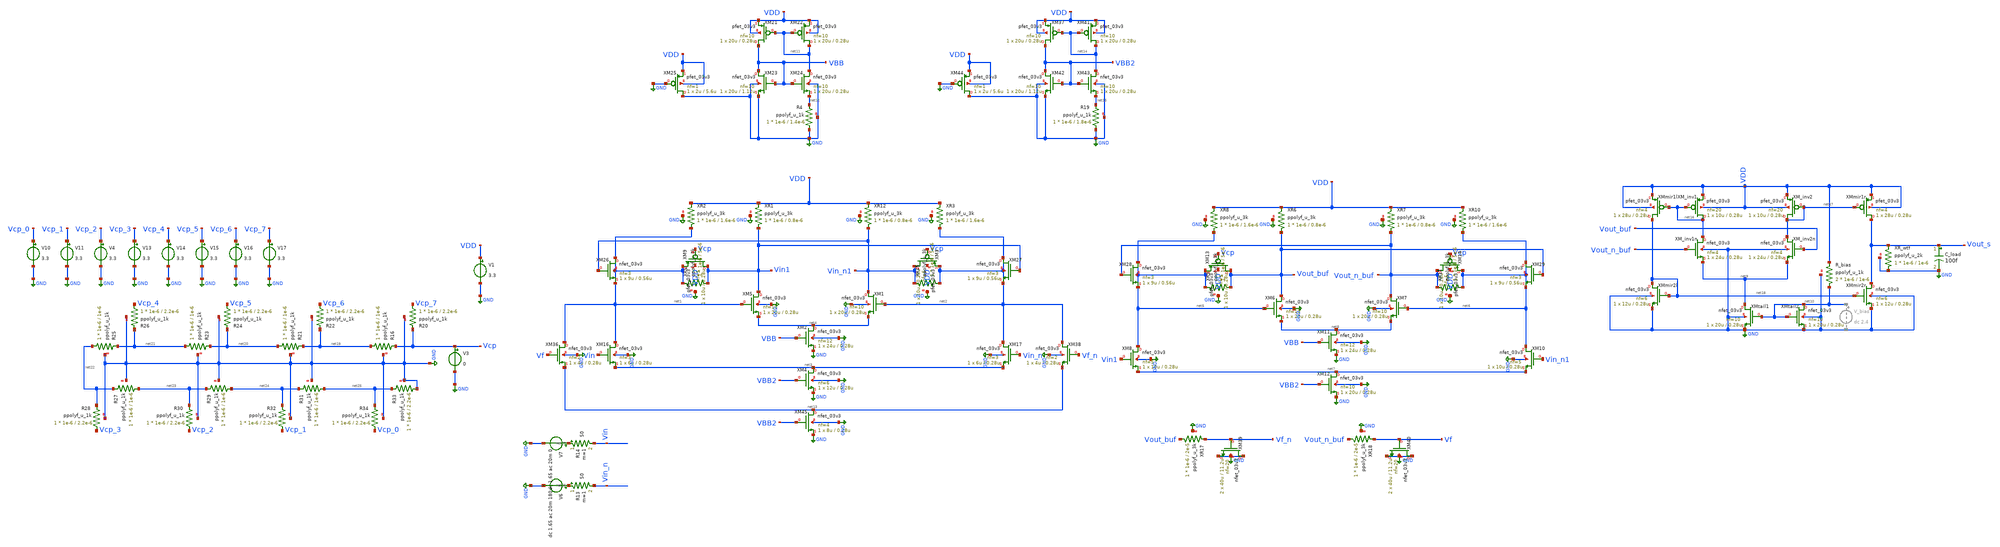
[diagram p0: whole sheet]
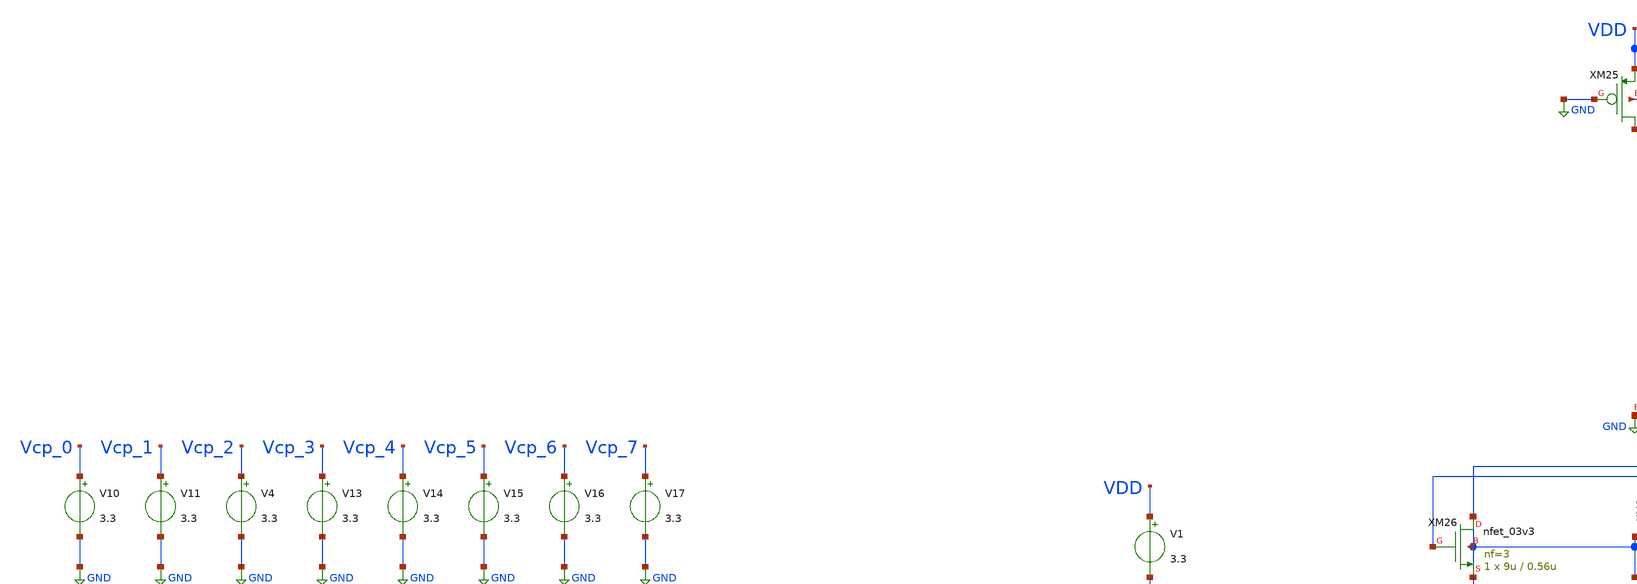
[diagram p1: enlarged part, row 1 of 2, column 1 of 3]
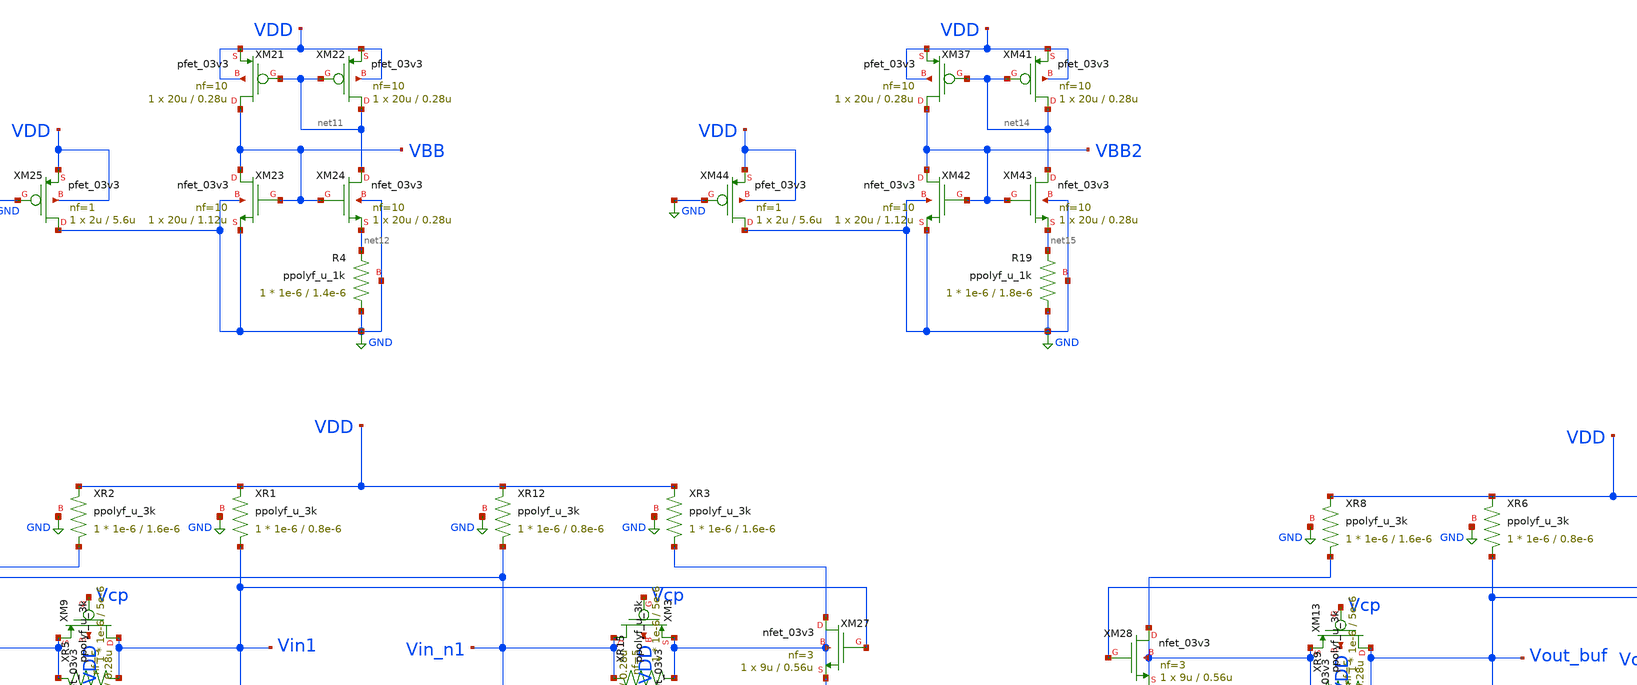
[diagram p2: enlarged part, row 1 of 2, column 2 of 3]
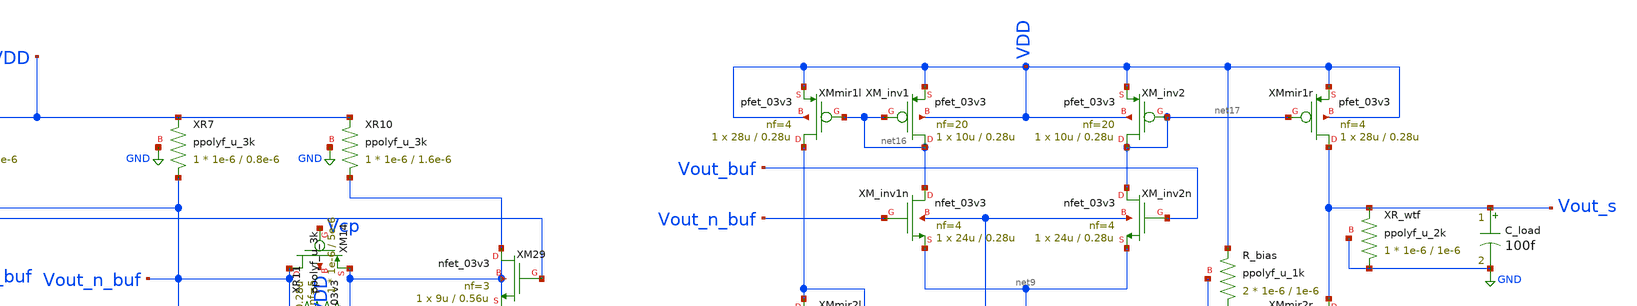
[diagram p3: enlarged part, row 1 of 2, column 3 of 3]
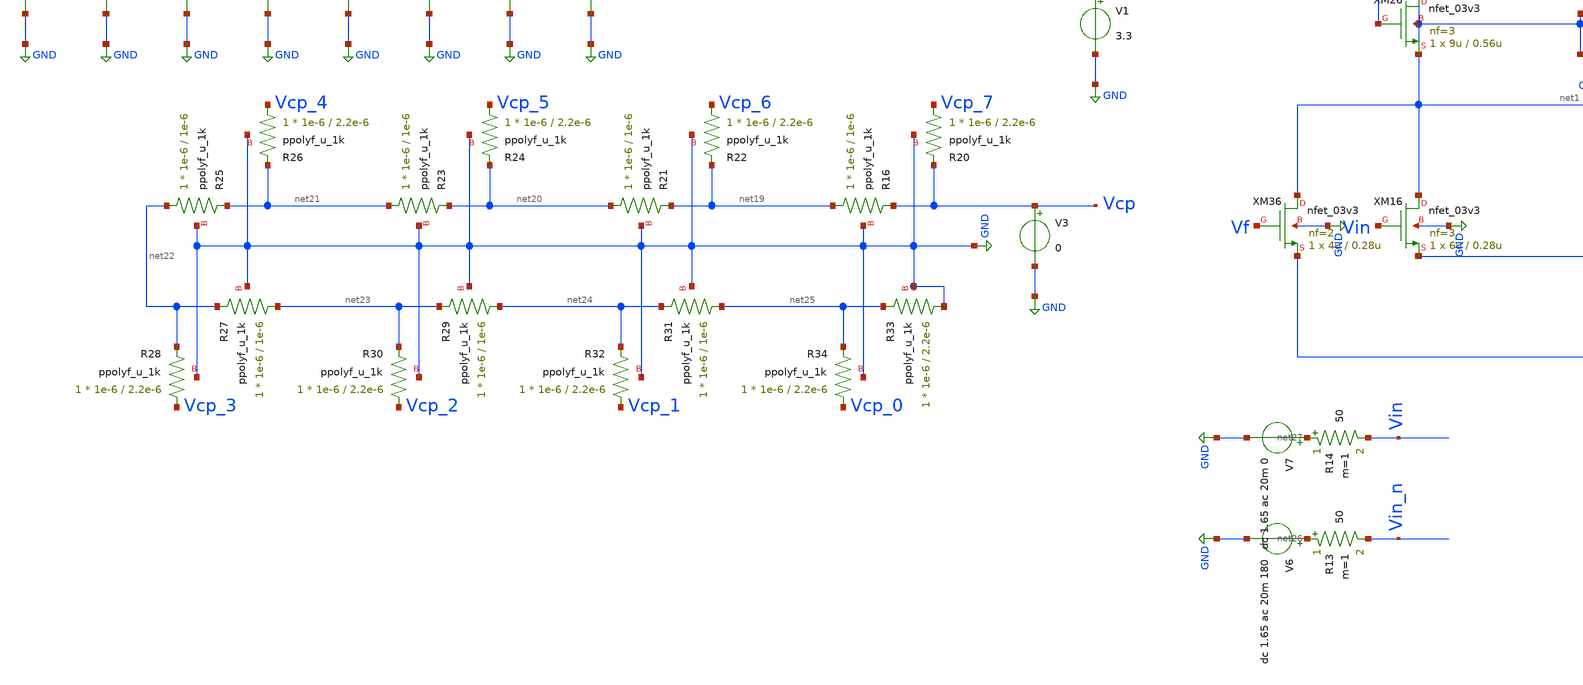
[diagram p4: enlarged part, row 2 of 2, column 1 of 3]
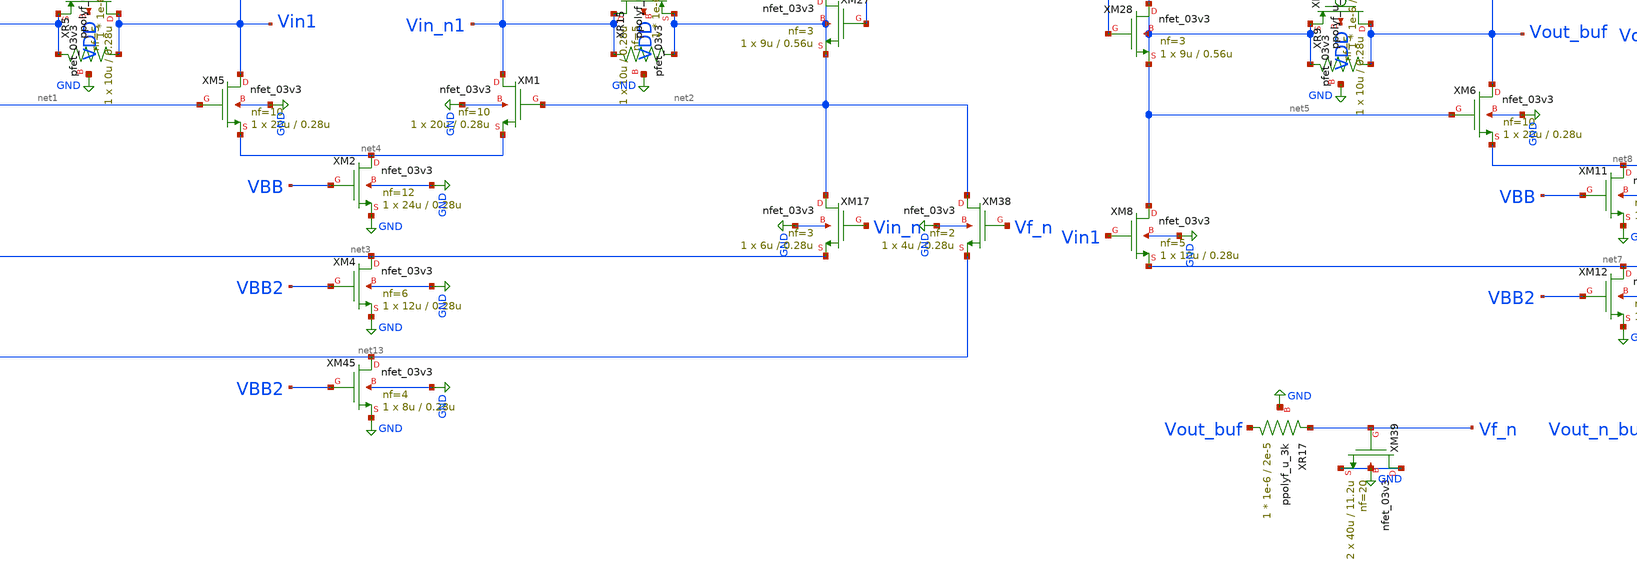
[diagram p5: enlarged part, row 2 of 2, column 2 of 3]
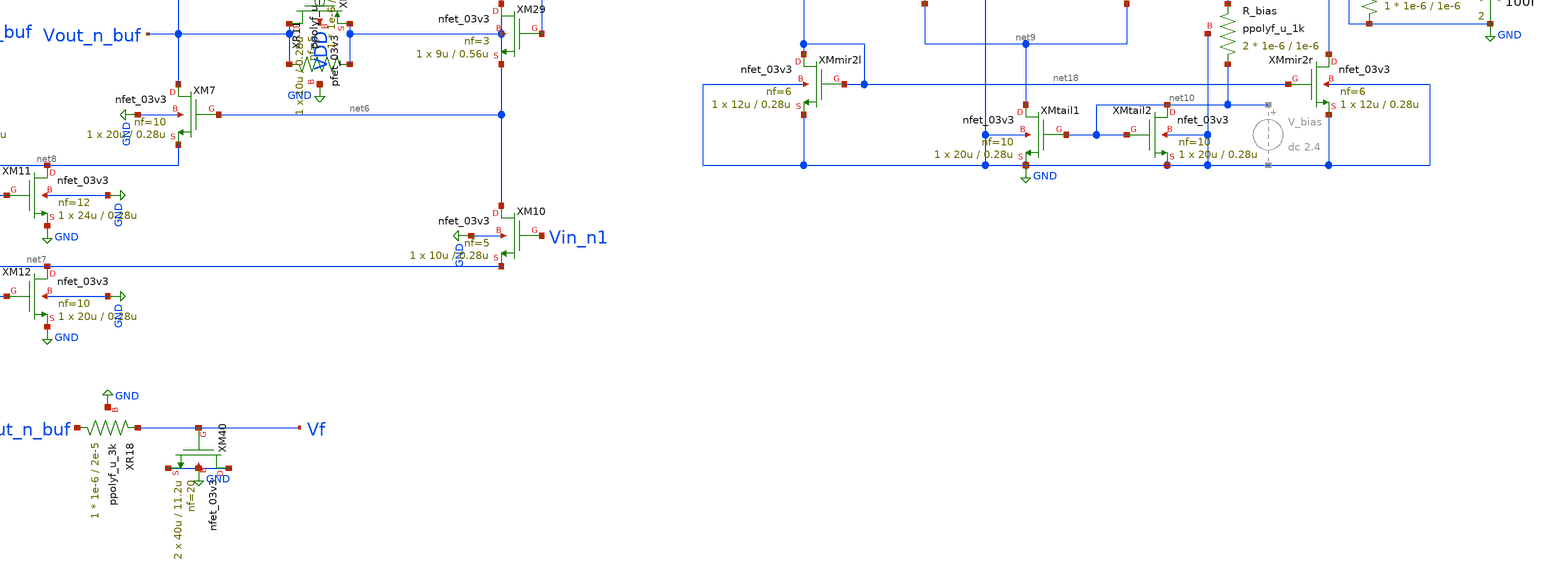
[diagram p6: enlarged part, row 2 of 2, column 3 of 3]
** sch_path: blocks/vga/vga.sch
**.subckt vga
V1 VDD GND 3.3
V6 net26 GND dc 1.65 ac 20m 180
XM5 Vin1 net1 net4 GND nfet_03v3 L=0.28u W=20u nf=10 ad='int((nf+1)/2) * W/nf * 0.18u' as='int((nf+2)/2) * W/nf * 0.18u'
+ pd='2*int((nf+1)/2) * (W/nf + 0.18u)' ps='2*int((nf+2)/2) * (W/nf + 0.18u)' nrd='0.18u / W' nrs='0.18u / W'
+ sa=0 sb=0 sd=0 m=1
XM1 Vin_n1 net2 net4 GND nfet_03v3 L=0.28u W=20u nf=10 ad='int((nf+1)/2) * W/nf * 0.18u' as='int((nf+2)/2) * W/nf * 0.18u'
+ pd='2*int((nf+1)/2) * (W/nf + 0.18u)' ps='2*int((nf+2)/2) * (W/nf + 0.18u)' nrd='0.18u / W' nrs='0.18u / W'
+ sa=0 sb=0 sd=0 m=1
XM16 net1 Vin net3 GND nfet_03v3 L=0.28u W=6u nf=3 ad='int((nf+1)/2) * W/nf * 0.18u' as='int((nf+2)/2) * W/nf * 0.18u'
+ pd='2*int((nf+1)/2) * (W/nf + 0.18u)' ps='2*int((nf+2)/2) * (W/nf + 0.18u)' nrd='0.18u / W' nrs='0.18u / W'
+ sa=0 sb=0 sd=0 m=1
XM17 net2 Vin_n net3 GND nfet_03v3 L=0.28u W=6u nf=3 ad='int((nf+1)/2) * W/nf * 0.18u' as='int((nf+2)/2) * W/nf * 0.18u'
+ pd='2*int((nf+1)/2) * (W/nf + 0.18u)' ps='2*int((nf+2)/2) * (W/nf + 0.18u)' nrd='0.18u / W' nrs='0.18u / W'
+ sa=0 sb=0 sd=0 m=1
XM2 net4 VBB GND GND nfet_03v3 L=0.28u W=24u nf=12 ad='int((nf+1)/2) * W/nf * 0.18u' as='int((nf+2)/2) * W/nf * 0.18u'
+ pd='2*int((nf+1)/2) * (W/nf + 0.18u)' ps='2*int((nf+2)/2) * (W/nf + 0.18u)' nrd='0.18u / W' nrs='0.18u / W'
+ sa=0 sb=0 sd=0 m=1
XM4 net3 VBB2 GND GND nfet_03v3 L=0.28u W=12u nf=6 ad='int((nf+1)/2) * W/nf * 0.18u' as='int((nf+2)/2) * W/nf * 0.18u'
+ pd='2*int((nf+1)/2) * (W/nf + 0.18u)' ps='2*int((nf+2)/2) * (W/nf + 0.18u)' nrd='0.18u / W' nrs='0.18u / W'
+ sa=0 sb=0 sd=0 m=1
XM9 Vin1 Vcp net1 VDD pfet_03v3 L=0.28u W=10u nf=5 ad='int((nf+1)/2) * W/nf * 0.18u' as='int((nf+2)/2) * W/nf * 0.18u'
+ pd='2*int((nf+1)/2) * (W/nf + 0.18u)' ps='2*int((nf+2)/2) * (W/nf + 0.18u)' nrd='0.18u / W' nrs='0.18u / W'
+ sa=0 sb=0 sd=0 m=1
XM3 Vin_n1 Vcp net2 VDD pfet_03v3 L=0.28u W=10u nf=5 ad='int((nf+1)/2) * W/nf * 0.18u' as='int((nf+2)/2) * W/nf * 0.18u'
+ pd='2*int((nf+1)/2) * (W/nf + 0.18u)' ps='2*int((nf+2)/2) * (W/nf + 0.18u)' nrd='0.18u / W' nrs='0.18u / W'
+ sa=0 sb=0 sd=0 m=1
XM6 Vout_buf net5 net8 GND nfet_03v3 L=0.28u W=20u nf=10 ad='int((nf+1)/2) * W/nf * 0.18u' as='int((nf+2)/2) * W/nf * 0.18u'
+ pd='2*int((nf+1)/2) * (W/nf + 0.18u)' ps='2*int((nf+2)/2) * (W/nf + 0.18u)' nrd='0.18u / W' nrs='0.18u / W'
+ sa=0 sb=0 sd=0 m=1
XM7 Vout_n_buf net6 net8 GND nfet_03v3 L=0.28u W=20u nf=10 ad='int((nf+1)/2) * W/nf * 0.18u' as='int((nf+2)/2) * W/nf * 0.18u'
+ pd='2*int((nf+1)/2) * (W/nf + 0.18u)' ps='2*int((nf+2)/2) * (W/nf + 0.18u)' nrd='0.18u / W' nrs='0.18u / W'
+ sa=0 sb=0 sd=0 m=1
XM8 net5 Vin1 net7 GND nfet_03v3 L=0.28u W=10u nf=5 ad='int((nf+1)/2) * W/nf * 0.18u' as='int((nf+2)/2) * W/nf * 0.18u'
+ pd='2*int((nf+1)/2) * (W/nf + 0.18u)' ps='2*int((nf+2)/2) * (W/nf + 0.18u)' nrd='0.18u / W' nrs='0.18u / W'
+ sa=0 sb=0 sd=0 m=1
XM10 net6 Vin_n1 net7 GND nfet_03v3 L=0.28u W=10u nf=5 ad='int((nf+1)/2) * W/nf * 0.18u' as='int((nf+2)/2) * W/nf * 0.18u'
+ pd='2*int((nf+1)/2) * (W/nf + 0.18u)' ps='2*int((nf+2)/2) * (W/nf + 0.18u)' nrd='0.18u / W' nrs='0.18u / W'
+ sa=0 sb=0 sd=0 m=1
XM11 net8 VBB GND GND nfet_03v3 L=0.28u W=24u nf=12 ad='int((nf+1)/2) * W/nf * 0.18u' as='int((nf+2)/2) * W/nf * 0.18u'
+ pd='2*int((nf+1)/2) * (W/nf + 0.18u)' ps='2*int((nf+2)/2) * (W/nf + 0.18u)' nrd='0.18u / W' nrs='0.18u / W'
+ sa=0 sb=0 sd=0 m=1
XM12 net7 VBB2 GND GND nfet_03v3 L=0.28u W=20u nf=10 ad='int((nf+1)/2) * W/nf * 0.18u' as='int((nf+2)/2) * W/nf * 0.18u'
+ pd='2*int((nf+1)/2) * (W/nf + 0.18u)' ps='2*int((nf+2)/2) * (W/nf + 0.18u)' nrd='0.18u / W' nrs='0.18u / W'
+ sa=0 sb=0 sd=0 m=1
XM13 Vout_buf Vcp net5 VDD pfet_03v3 L=0.28u W=10u nf=5 ad='int((nf+1)/2) * W/nf * 0.18u' as='int((nf+2)/2) * W/nf * 0.18u'
+ pd='2*int((nf+1)/2) * (W/nf + 0.18u)' ps='2*int((nf+2)/2) * (W/nf + 0.18u)' nrd='0.18u / W' nrs='0.18u / W'
+ sa=0 sb=0 sd=0 m=1
XM14 Vout_n_buf Vcp net6 VDD pfet_03v3 L=0.28u W=10u nf=5 ad='int((nf+1)/2) * W/nf * 0.18u' as='int((nf+2)/2) * W/nf * 0.18u'
+ pd='2*int((nf+1)/2) * (W/nf + 0.18u)' ps='2*int((nf+2)/2) * (W/nf + 0.18u)' nrd='0.18u / W' nrs='0.18u / W'
+ sa=0 sb=0 sd=0 m=1
V7 net27 GND dc 1.65 ac 20m 0
R14 net27 Vin 50 m=1
R13 net26 Vin_n 50 m=1
XM21 VBB net11 VDD VDD pfet_03v3 L=0.28u W=20u nf=10 ad='int((nf+1)/2) * W/nf * 0.18u' as='int((nf+2)/2) * W/nf * 0.18u'
+ pd='2*int((nf+1)/2) * (W/nf + 0.18u)' ps='2*int((nf+2)/2) * (W/nf + 0.18u)' nrd='0.18u / W' nrs='0.18u / W'
+ sa=0 sb=0 sd=0 m=1
XM22 net11 net11 VDD VDD pfet_03v3 L=0.28u W=20u nf=10 ad='int((nf+1)/2) * W/nf * 0.18u' as='int((nf+2)/2) * W/nf * 0.18u'
+ pd='2*int((nf+1)/2) * (W/nf + 0.18u)' ps='2*int((nf+2)/2) * (W/nf + 0.18u)' nrd='0.18u / W' nrs='0.18u / W'
+ sa=0 sb=0 sd=0 m=1
XM23 VBB VBB GND GND nfet_03v3 L=1.12u W=20u nf=10 ad='int((nf+1)/2) * W/nf * 0.18u' as='int((nf+2)/2) * W/nf * 0.18u'
+ pd='2*int((nf+1)/2) * (W/nf + 0.18u)' ps='2*int((nf+2)/2) * (W/nf + 0.18u)' nrd='0.18u / W' nrs='0.18u / W'
+ sa=0 sb=0 sd=0 m=1
XM24 net11 VBB net12 GND nfet_03v3 L=0.28u W=20u nf=10 ad='int((nf+1)/2) * W/nf * 0.18u' as='int((nf+2)/2) * W/nf * 0.18u'
+ pd='2*int((nf+1)/2) * (W/nf + 0.18u)' ps='2*int((nf+2)/2) * (W/nf + 0.18u)' nrd='0.18u / W' nrs='0.18u / W'
+ sa=0 sb=0 sd=0 m=1
XM25 GND GND VDD VDD pfet_03v3 L=5.6u W=2u nf=1 ad='int((nf+1)/2) * W/nf * 0.18u' as='int((nf+2)/2) * W/nf * 0.18u'
+ pd='2*int((nf+1)/2) * (W/nf + 0.18u)' ps='2*int((nf+2)/2) * (W/nf + 0.18u)' nrd='0.18u / W' nrs='0.18u / W'
+ sa=0 sb=0 sd=0 m=1
XR5 Vin1 net1 GND ppolyf_u_3k r_width=1e-6 r_length=5e-6 m=1
XR15 net2 Vin_n1 GND ppolyf_u_3k r_width=1e-6 r_length=5e-6 m=1
XR2 net1 VDD GND ppolyf_u_3k r_width=1e-6 r_length=1.6e-6 m=1
XR3 net2 VDD GND ppolyf_u_3k r_width=1e-6 r_length=1.6e-6 m=1
XR4 GND net12 GND ppolyf_u_1k r_width=1e-6 r_length=1.4e-6 m=1
XR1 Vin1 VDD GND ppolyf_u_3k r_width=1e-6 r_length=0.8e-6 m=1
XR12 Vin_n1 VDD GND ppolyf_u_3k r_width=1e-6 r_length=0.8e-6 m=1
XR6 Vout_buf VDD GND ppolyf_u_3k r_width=1e-6 r_length=0.8e-6 m=1
XR7 Vout_n_buf VDD GND ppolyf_u_3k r_width=1e-6 r_length=0.8e-6 m=1
XR9 Vout_buf net5 GND ppolyf_u_3k r_width=1e-6 r_length=5e-6 m=1
XR11 net6 Vout_n_buf GND ppolyf_u_3k r_width=1e-6 r_length=5e-6 m=1
XR8 net5 VDD GND ppolyf_u_3k r_width=1e-6 r_length=1.6e-6 m=1
XR10 net6 VDD GND ppolyf_u_3k r_width=1e-6 r_length=1.6e-6 m=1
XM26 net1 Vin_n1 net1 net1 nfet_03v3 L=0.56u W=9u nf=3 ad='int((nf+1)/2) * W/nf * 0.18u' as='int((nf+2)/2) * W/nf * 0.18u'
+ pd='2*int((nf+1)/2) * (W/nf + 0.18u)' ps='2*int((nf+2)/2) * (W/nf + 0.18u)' nrd='0.18u / W' nrs='0.18u / W'
+ sa=0 sb=0 sd=0 m=1
XM27 net2 Vin1 net2 net2 nfet_03v3 L=0.56u W=9u nf=3 ad='int((nf+1)/2) * W/nf * 0.18u' as='int((nf+2)/2) * W/nf * 0.18u'
+ pd='2*int((nf+1)/2) * (W/nf + 0.18u)' ps='2*int((nf+2)/2) * (W/nf + 0.18u)' nrd='0.18u / W' nrs='0.18u / W'
+ sa=0 sb=0 sd=0 m=1
XM28 net5 Vout_n_buf net5 net5 nfet_03v3 L=0.56u W=9u nf=3 ad='int((nf+1)/2) * W/nf * 0.18u' as='int((nf+2)/2) * W/nf * 0.18u'
+ pd='2*int((nf+1)/2) * (W/nf + 0.18u)' ps='2*int((nf+2)/2) * (W/nf + 0.18u)' nrd='0.18u / W' nrs='0.18u / W'
+ sa=0 sb=0 sd=0 m=1
XM29 net6 Vout_buf net6 net6 nfet_03v3 L=0.56u W=9u nf=3 ad='int((nf+1)/2) * W/nf * 0.18u' as='int((nf+2)/2) * W/nf * 0.18u'
+ pd='2*int((nf+1)/2) * (W/nf + 0.18u)' ps='2*int((nf+2)/2) * (W/nf + 0.18u)' nrd='0.18u / W' nrs='0.18u / W'
+ sa=0 sb=0 sd=0 m=1
XM_inv1 net16 net16 VDD VDD pfet_03v3 L=0.28u W=10u nf=20 ad='int((nf+1)/2) * W/nf * 0.18u' as='int((nf+2)/2) * W/nf * 0.18u'
+ pd='2*int((nf+1)/2) * (W/nf + 0.18u)' ps='2*int((nf+2)/2) * (W/nf + 0.18u)' nrd='0.18u / W' nrs='0.18u / W'
+ sa=0 sb=0 sd=0 m=1
XM_inv1n net16 Vout_n_buf net9 GND nfet_03v3 L=0.28u W=24u nf=4 ad='int((nf+1)/2) * W/nf * 0.18u' as='int((nf+2)/2) * W/nf * 0.18u'
+ pd='2*int((nf+1)/2) * (W/nf + 0.18u)' ps='2*int((nf+2)/2) * (W/nf + 0.18u)' nrd='0.18u / W' nrs='0.18u / W'
+ sa=0 sb=0 sd=0 m=1
XM_inv2 net17 net17 VDD VDD pfet_03v3 L=0.28u W=10u nf=20 ad='int((nf+1)/2) * W/nf * 0.18u' as='int((nf+2)/2) * W/nf * 0.18u'
+ pd='2*int((nf+1)/2) * (W/nf + 0.18u)' ps='2*int((nf+2)/2) * (W/nf + 0.18u)' nrd='0.18u / W' nrs='0.18u / W'
+ sa=0 sb=0 sd=0 m=1
XM_inv2n net17 Vout_buf net9 GND nfet_03v3 L=0.28u W=24u nf=4 ad='int((nf+1)/2) * W/nf * 0.18u' as='int((nf+2)/2) * W/nf * 0.18u'
+ pd='2*int((nf+1)/2) * (W/nf + 0.18u)' ps='2*int((nf+2)/2) * (W/nf + 0.18u)' nrd='0.18u / W' nrs='0.18u / W'
+ sa=0 sb=0 sd=0 m=1
XMtail1 net9 net10 GND GND nfet_03v3 L=0.28u W=20u nf=10 ad='int((nf+1)/2) * W/nf * 0.18u' as='int((nf+2)/2) * W/nf * 0.18u'
+ pd='2*int((nf+1)/2) * (W/nf + 0.18u)' ps='2*int((nf+2)/2) * (W/nf + 0.18u)' nrd='0.18u / W' nrs='0.18u / W'
+ sa=0 sb=0 sd=0 m=1
XMtail2 net10 net10 GND GND nfet_03v3 L=0.28u W=20u nf=10 ad='int((nf+1)/2) * W/nf * 0.18u' as='int((nf+2)/2) * W/nf * 0.18u'
+ pd='2*int((nf+1)/2) * (W/nf + 0.18u)' ps='2*int((nf+2)/2) * (W/nf + 0.18u)' nrd='0.18u / W' nrs='0.18u / W'
+ sa=0 sb=0 sd=0 m=1
XM36 net1 Vf net13 GND nfet_03v3 L=0.28u W=4u nf=2 ad='int((nf+1)/2) * W/nf * 0.18u' as='int((nf+2)/2) * W/nf * 0.18u'
+ pd='2*int((nf+1)/2) * (W/nf + 0.18u)' ps='2*int((nf+2)/2) * (W/nf + 0.18u)' nrd='0.18u / W' nrs='0.18u / W'
+ sa=0 sb=0 sd=0 m=1
XM38 net2 Vf_n net13 GND nfet_03v3 L=0.28u W=4u nf=2 ad='int((nf+1)/2) * W/nf * 0.18u' as='int((nf+2)/2) * W/nf * 0.18u'
+ pd='2*int((nf+1)/2) * (W/nf + 0.18u)' ps='2*int((nf+2)/2) * (W/nf + 0.18u)' nrd='0.18u / W' nrs='0.18u / W'
+ sa=0 sb=0 sd=0 m=1
XR17 Vout_buf Vf_n GND ppolyf_u_3k r_width=1e-6 r_length=2e-5 m=1
XM39 GND Vf_n GND GND nfet_03v3 L=11.2u W=40u nf=20 ad='int((nf+1)/2) * W/nf * 0.18u' as='int((nf+2)/2) * W/nf * 0.18u'
+ pd='2*int((nf+1)/2) * (W/nf + 0.18u)' ps='2*int((nf+2)/2) * (W/nf + 0.18u)' nrd='0.18u / W' nrs='0.18u / W'
+ sa=0 sb=0 sd=0 m=2
XR18 Vout_n_buf Vf GND ppolyf_u_3k r_width=1e-6 r_length=2e-5 m=1
XM40 GND Vf GND GND nfet_03v3 L=11.2u W=40u nf=20 ad='int((nf+1)/2) * W/nf * 0.18u' as='int((nf+2)/2) * W/nf * 0.18u'
+ pd='2*int((nf+1)/2) * (W/nf + 0.18u)' ps='2*int((nf+2)/2) * (W/nf + 0.18u)' nrd='0.18u / W' nrs='0.18u / W'
+ sa=0 sb=0 sd=0 m=2
XM37 VBB2 net14 VDD VDD pfet_03v3 L=0.28u W=20u nf=10 ad='int((nf+1)/2) * W/nf * 0.18u' as='int((nf+2)/2) * W/nf * 0.18u'
+ pd='2*int((nf+1)/2) * (W/nf + 0.18u)' ps='2*int((nf+2)/2) * (W/nf + 0.18u)' nrd='0.18u / W' nrs='0.18u / W'
+ sa=0 sb=0 sd=0 m=1
XM41 net14 net14 VDD VDD pfet_03v3 L=0.28u W=20u nf=10 ad='int((nf+1)/2) * W/nf * 0.18u' as='int((nf+2)/2) * W/nf * 0.18u'
+ pd='2*int((nf+1)/2) * (W/nf + 0.18u)' ps='2*int((nf+2)/2) * (W/nf + 0.18u)' nrd='0.18u / W' nrs='0.18u / W'
+ sa=0 sb=0 sd=0 m=1
XM42 VBB2 VBB2 GND GND nfet_03v3 L=1.12u W=20u nf=10 ad='int((nf+1)/2) * W/nf * 0.18u' as='int((nf+2)/2) * W/nf * 0.18u'
+ pd='2*int((nf+1)/2) * (W/nf + 0.18u)' ps='2*int((nf+2)/2) * (W/nf + 0.18u)' nrd='0.18u / W' nrs='0.18u / W'
+ sa=0 sb=0 sd=0 m=1
XM43 net14 VBB2 net15 GND nfet_03v3 L=0.28u W=20u nf=10 ad='int((nf+1)/2) * W/nf * 0.18u' as='int((nf+2)/2) * W/nf * 0.18u'
+ pd='2*int((nf+1)/2) * (W/nf + 0.18u)' ps='2*int((nf+2)/2) * (W/nf + 0.18u)' nrd='0.18u / W' nrs='0.18u / W'
+ sa=0 sb=0 sd=0 m=1
XM44 GND GND VDD VDD pfet_03v3 L=5.6u W=2u nf=1 ad='int((nf+1)/2) * W/nf * 0.18u' as='int((nf+2)/2) * W/nf * 0.18u'
+ pd='2*int((nf+1)/2) * (W/nf + 0.18u)' ps='2*int((nf+2)/2) * (W/nf + 0.18u)' nrd='0.18u / W' nrs='0.18u / W'
+ sa=0 sb=0 sd=0 m=1
XR19 GND net15 GND ppolyf_u_1k r_width=1e-6 r_length=1.8e-6 m=1
XM45 net13 VBB2 GND GND nfet_03v3 L=0.28u W=8u nf=4 ad='int((nf+1)/2) * W/nf * 0.18u' as='int((nf+2)/2) * W/nf * 0.18u'
+ pd='2*int((nf+1)/2) * (W/nf + 0.18u)' ps='2*int((nf+2)/2) * (W/nf + 0.18u)' nrd='0.18u / W' nrs='0.18u / W'
+ sa=0 sb=0 sd=0 m=1
XMmir1l net18 net16 VDD VDD pfet_03v3 L=0.28u W=28u nf=4 ad='int((nf+1)/2) * W/nf * 0.18u' as='int((nf+2)/2) * W/nf * 0.18u'
+ pd='2*int((nf+1)/2) * (W/nf + 0.18u)' ps='2*int((nf+2)/2) * (W/nf + 0.18u)' nrd='0.18u / W' nrs='0.18u / W'
+ sa=0 sb=0 sd=0 m=1
XMmir1r Vout_s net17 VDD VDD pfet_03v3 L=0.28u W=28u nf=4 ad='int((nf+1)/2) * W/nf * 0.18u' as='int((nf+2)/2) * W/nf * 0.18u'
+ pd='2*int((nf+1)/2) * (W/nf + 0.18u)' ps='2*int((nf+2)/2) * (W/nf + 0.18u)' nrd='0.18u / W' nrs='0.18u / W'
+ sa=0 sb=0 sd=0 m=1
XMmir2l net18 net18 GND GND nfet_03v3 L=0.28u W=12u nf=6 ad='int((nf+1)/2) * W/nf * 0.18u' as='int((nf+2)/2) * W/nf * 0.18u'
+ pd='2*int((nf+1)/2) * (W/nf + 0.18u)' ps='2*int((nf+2)/2) * (W/nf + 0.18u)' nrd='0.18u / W' nrs='0.18u / W'
+ sa=0 sb=0 sd=0 m=1
XMmir2r Vout_s net18 GND GND nfet_03v3 L=0.28u W=12u nf=6 ad='int((nf+1)/2) * W/nf * 0.18u' as='int((nf+2)/2) * W/nf * 0.18u'
+ pd='2*int((nf+1)/2) * (W/nf + 0.18u)' ps='2*int((nf+2)/2) * (W/nf + 0.18u)' nrd='0.18u / W' nrs='0.18u / W'
+ sa=0 sb=0 sd=0 m=1
XR_bias net10 VDD GND ppolyf_u_1k r_width=1e-6 r_length=1e-6 m=2
C_load Vout_s GND 100f m=1
XR_wtf GND Vout_s GND ppolyf_u_2k r_width=1e-6 r_length=1e-6 m=1
XR16 net19 Vcp GND ppolyf_u_1k r_width=1e-6 r_length=1e-6 m=1
XR20 Vcp_7 Vcp GND ppolyf_u_1k r_width=1e-6 r_length=2.2e-6 m=1
XR21 net20 net19 GND ppolyf_u_1k r_width=1e-6 r_length=1e-6 m=1
XR22 Vcp_6 net19 GND ppolyf_u_1k r_width=1e-6 r_length=2.2e-6 m=1
XR23 net21 net20 GND ppolyf_u_1k r_width=1e-6 r_length=1e-6 m=1
XR24 Vcp_5 net20 GND ppolyf_u_1k r_width=1e-6 r_length=2.2e-6 m=1
XR25 net22 net21 GND ppolyf_u_1k r_width=1e-6 r_length=1e-6 m=1
XR26 Vcp_4 net21 GND ppolyf_u_1k r_width=1e-6 r_length=2.2e-6 m=1
XR27 net23 net22 GND ppolyf_u_1k r_width=1e-6 r_length=1e-6 m=1
XR28 Vcp_3 net22 GND ppolyf_u_1k r_width=1e-6 r_length=2.2e-6 m=1
XR29 net24 net23 GND ppolyf_u_1k r_width=1e-6 r_length=1e-6 m=1
XR30 Vcp_2 net23 GND ppolyf_u_1k r_width=1e-6 r_length=2.2e-6 m=1
XR31 net25 net24 GND ppolyf_u_1k r_width=1e-6 r_length=1e-6 m=1
XR32 Vcp_1 net24 GND ppolyf_u_1k r_width=1e-6 r_length=2.2e-6 m=1
XR33 GND net25 GND ppolyf_u_1k r_width=1e-6 r_length=2.2e-6 m=1
XR34 Vcp_0 net25 GND ppolyf_u_1k r_width=1e-6 r_length=2.2e-6 m=1
V10 Vcp_0 GND 3.3
V11 Vcp_1 GND 3.3
V4 Vcp_2 GND 3.3
V13 Vcp_3 GND 3.3
V14 Vcp_4 GND 3.3
V15 Vcp_5 GND 3.3
V16 Vcp_6 GND 3.3
V17 Vcp_7 GND 3.3
V3 Vcp GND 0
**** begin user architecture code


.include /foss/pdks/gf180mcuD/libs.tech/ngspice/design.ngspice
.lib /foss/pdks/gf180mcuD/libs.tech/ngspice/sm141064.ngspice ss
.lib /foss/pdks/gf180mcuD/libs.tech/ngspice/sm141064.ngspice res_ss
.option method=gear

.control
set temp = -40
  * 1. Setup the sweep parameters
  let v_start = 0
  let v_stop = 3.3
  let v_points = 66
  let v_delta = (v_stop - v_start) / v_points

  * 2. Initialize vectors to store results
  let gain_db_20 = unitvec(v_points + 1)
  let gain_db_1200 = unitvec(v_points + 1)
  let vcp_axis = unitvec(v_points + 1)

  let i = 0
  while i <= v_points
    let v_current = v_start + (i * v_delta)
    alter v3 = v_current   ; Adjust the Vcp source DC value

    * 3. Run AC analysis ONLY at 600MHz to maximize speed
    ac lin 3 0.02G 1.2G

    * 4. Calculate Differential Gain in dB
    * Formula: 20 * log10(|Vout_diff| / |Vin_diff|)
    * let vout_mag = mag(v(vout_buf) - v(vout_n_buf))
    let vout_mag = mag(v(vout_s))
    let vin_mag = mag(v(vin) - v(vin_n))
    let g_val = 20 * log10(vout_mag / vin_mag)

    * 5. Save results to vectors
    let gain_db_20[i] = g_val[1]
    let gain_db_1200[i] = g_val[2]
    let vcp_axis[i] = v_current
    let i = i + 1
    *print mag(v(vout) - v(vout_n))
    *print i(v1)
  end

  * 6. Plot the Gain vs Control Voltage
  plot gain_db_20 gain_db_1200 vs vcp_axis title 'VGA Gain at 20MHz, 1.2GHz vs Vcp, 100fF load' xlabel
+ 'Vcp (V)' ylabel 'Gain (dB)'
.endc


**** end user architecture code
**.ends
.GLOBAL GND
.end
